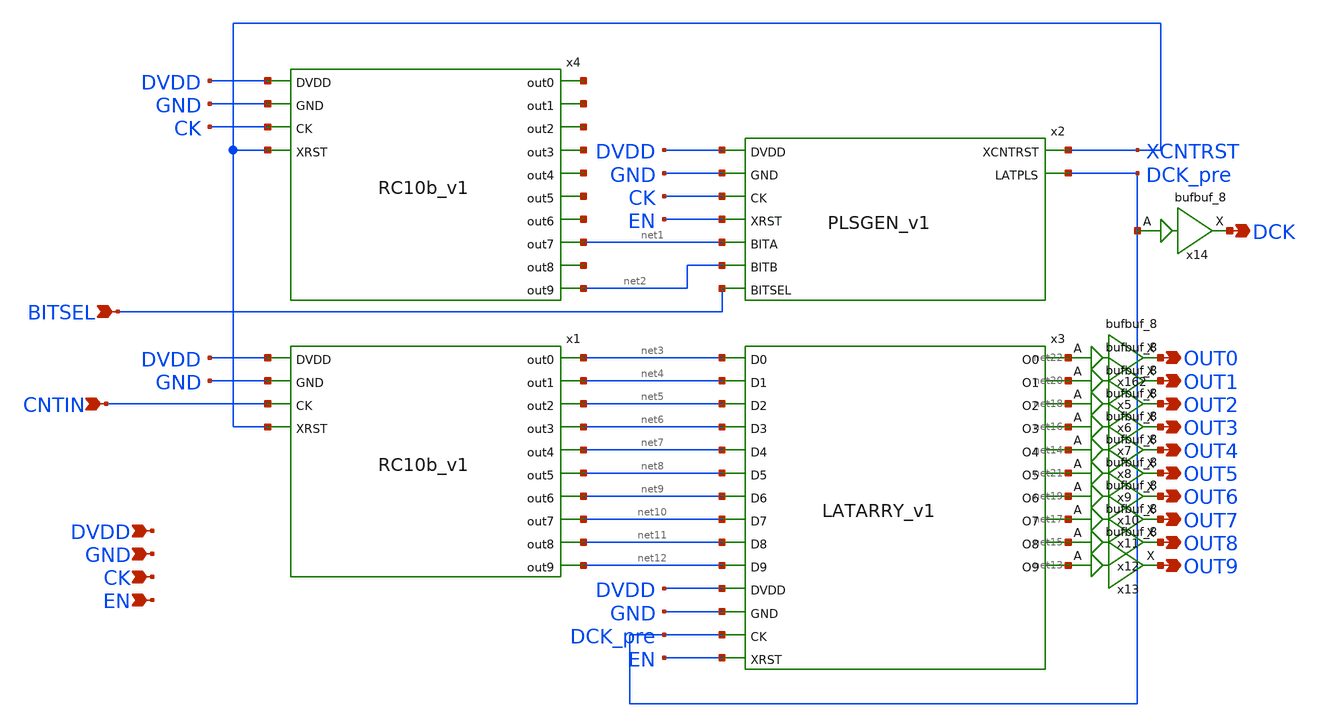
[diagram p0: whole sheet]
** sch_path: design/schematic/CNTDIG_v1.sch
**.subckt CNTDIG_v1 CK EN DVDD GND CNTIN BITSEL OUT0 OUT1 OUT2 OUT3 OUT4 OUT5 OUT6 OUT7 OUT8 OUT9
*+ DCK
*.ipin CK
*.ipin EN
*.ipin DVDD
*.ipin GND
*.ipin CNTIN
*.ipin BITSEL
*.opin OUT0
*.opin OUT1
*.opin OUT2
*.opin OUT3
*.opin OUT4
*.opin OUT5
*.opin OUT6
*.opin OUT7
*.opin OUT8
*.opin OUT9
*.opin DCK
x2 DVDD GND CK EN net1 net2 XCNTRST BITSEL DCK_pre PLSGEN_v1
x3 net13 net14 net12 net7 net15 net16 net11 net6 net17 net18 net10 net5 net19 net20 net9 net4 net21
+ net22 net8 DVDD net3 GND DCK_pre EN LATARRY_v1
x1 DVDD GND net10 net12 net5 net11 net8 net9 net7 net6 CNTIN net4 net3 XCNTRST RC10b_v1
x4 DVDD GND net1 net2 net23 net24 net25 net26 net27 net28 CK net29 net30 XCNTRST RC10b_v1
x162 net22 GND GND DVDD DVDD OUT0 sky130_fd_sc_hd__bufbuf_8
x5 net20 GND GND DVDD DVDD OUT1 sky130_fd_sc_hd__bufbuf_8
x6 net18 GND GND DVDD DVDD OUT2 sky130_fd_sc_hd__bufbuf_8
x7 net16 GND GND DVDD DVDD OUT3 sky130_fd_sc_hd__bufbuf_8
x8 net14 GND GND DVDD DVDD OUT4 sky130_fd_sc_hd__bufbuf_8
x9 net21 GND GND DVDD DVDD OUT5 sky130_fd_sc_hd__bufbuf_8
x10 net19 GND GND DVDD DVDD OUT6 sky130_fd_sc_hd__bufbuf_8
x11 net17 GND GND DVDD DVDD OUT7 sky130_fd_sc_hd__bufbuf_8
x12 net15 GND GND DVDD DVDD OUT8 sky130_fd_sc_hd__bufbuf_8
x13 net13 GND GND DVDD DVDD OUT9 sky130_fd_sc_hd__bufbuf_8
x14 DCK_pre GND GND DVDD DVDD DCK sky130_fd_sc_hd__bufbuf_8
**.ends

* expanding   symbol:  /home/ttuser/TT_WORK/rel/PLSGEN_v1.sym # of pins=9
** sym_path: design/schematic/PLSGEN_v1.sym
** sch_path: design/schematic/PLSGEN_v1.sch
.subckt PLSGEN_v1 DVDD GND CK XRST BITA BITB XCNTRST BITSEL LATPLS
*.ipin CK
*.ipin XRST
*.ipin DVDD
*.ipin GND
*.ipin BITA
*.ipin BITB
*.ipin BITSEL
*.opin XCNTRST
*.opin LATPLS
x8 CK net3 XRST GND GND DVDD DVDD net2 net6 sky130_fd_sc_hd__dfrbp_1
x102 net2 net3 GND GND DVDD DVDD net5 sky130_fd_sc_hd__xnor2_1
x46 BITA BITB BITSEL GND GND DVDD DVDD net1 sky130_fd_sc_hd__mux2_1
x9 DVDD GND net7 net4 net1 XRST TFF_v1
x11 DVDD GND net3 net8 net4 XRST TFF_v1
x12 CK net5 XRST GND GND DVDD DVDD XCNTRST net9 sky130_fd_sc_hd__dfrbp_1
x50 net5 GND GND DVDD DVDD LATPLS sky130_fd_sc_hd__inv_1
.ends


* expanding   symbol:  /home/ttuser/TT_WORK/rel/LATARRY_v1.sym # of pins=24
** sym_path: design/schematic/LATARRY_v1.sym
** sch_path: design/schematic/LATARRY_v1.sch
.subckt LATARRY_v1 O9 O4 D9 D4 O8 O3 D8 D3 O7 O2 D7 D2 O6 O1 D6 D1 O5 O0 D5 DVDD D0 GND CK XRST
*.ipin CK
*.ipin XRST
*.ipin DVDD
*.ipin GND
*.ipin D0
*.opin O0
*.ipin D1
*.opin O1
*.ipin D2
*.opin O2
*.ipin D3
*.opin O3
*.ipin D4
*.opin O4
*.ipin D5
*.opin O5
*.ipin D7
*.opin O7
*.ipin D8
*.opin O6
*.ipin D6
*.opin O8
*.ipin D9
*.opin O9
x0 CK D0 XRST GND GND DVDD DVDD O0 net1 sky130_fd_sc_hd__dfrbp_1
x1 CK D1 XRST GND GND DVDD DVDD O1 net2 sky130_fd_sc_hd__dfrbp_1
x2 CK D2 XRST GND GND DVDD DVDD O2 net3 sky130_fd_sc_hd__dfrbp_1
x3 CK D3 XRST GND GND DVDD DVDD O3 net4 sky130_fd_sc_hd__dfrbp_1
x4 CK D4 XRST GND GND DVDD DVDD O4 net5 sky130_fd_sc_hd__dfrbp_1
x5 CK D5 XRST GND GND DVDD DVDD O5 net6 sky130_fd_sc_hd__dfrbp_1
x6 CK D6 XRST GND GND DVDD DVDD O6 net7 sky130_fd_sc_hd__dfrbp_1
x7 CK D7 XRST GND GND DVDD DVDD O7 net8 sky130_fd_sc_hd__dfrbp_1
x8 CK D8 XRST GND GND DVDD DVDD O8 net9 sky130_fd_sc_hd__dfrbp_1
x9 CK D9 XRST GND GND DVDD DVDD O9 net10 sky130_fd_sc_hd__dfrbp_1
.ends


* expanding   symbol:  /home/ttuser/TT_WORK/rel/RC10b_v1.sym # of pins=14
** sym_path: design/schematic/RC10b_v1.sym
** sch_path: design/schematic/RC10b_v1.sch
.subckt RC10b_v1 DVDD GND out7 out9 out2 out8 out5 out6 out4 out3 CK out1 out0 XRST
*.ipin CK
*.ipin XRST
*.ipin DVDD
*.ipin GND
*.opin out9
*.opin out7
*.opin out8
*.opin out6
*.opin out5
*.opin out4
*.opin out3
*.opin out2
*.opin out1
*.opin out0
x0 DVDD GND net1 out0 CK XRST TFF_v1
x1 DVDD GND net2 out1 out0 XRST TFF_v1
x2 DVDD GND net3 out2 out1 XRST TFF_v1
x3 DVDD GND net4 out3 out2 XRST TFF_v1
x4 DVDD GND net5 out4 out3 XRST TFF_v1
x5 DVDD GND net6 out5 out4 XRST TFF_v1
x6 DVDD GND net7 out6 out5 XRST TFF_v1
x7 DVDD GND net8 out7 out6 XRST TFF_v1
x8 DVDD GND net9 out8 out7 XRST TFF_v1
x9 DVDD GND net10 out9 out8 XRST TFF_v1
.ends


* expanding   symbol:  /home/ttuser/TT_WORK/rel/TFF_v1.sym # of pins=6
** sym_path: design/schematic/TFF_v1.sym
** sch_path: design/schematic/TFF_v1.sch
.subckt TFF_v1 DVDD GND XQ Q CK XRST
*.ipin CK
*.ipin XRST
*.opin XQ
*.opin Q
*.ipin DVDD
*.ipin GND
x0 CK XQ XRST GND GND DVDD DVDD Q XQ sky130_fd_sc_hd__dfrbp_1
.ends

.end
